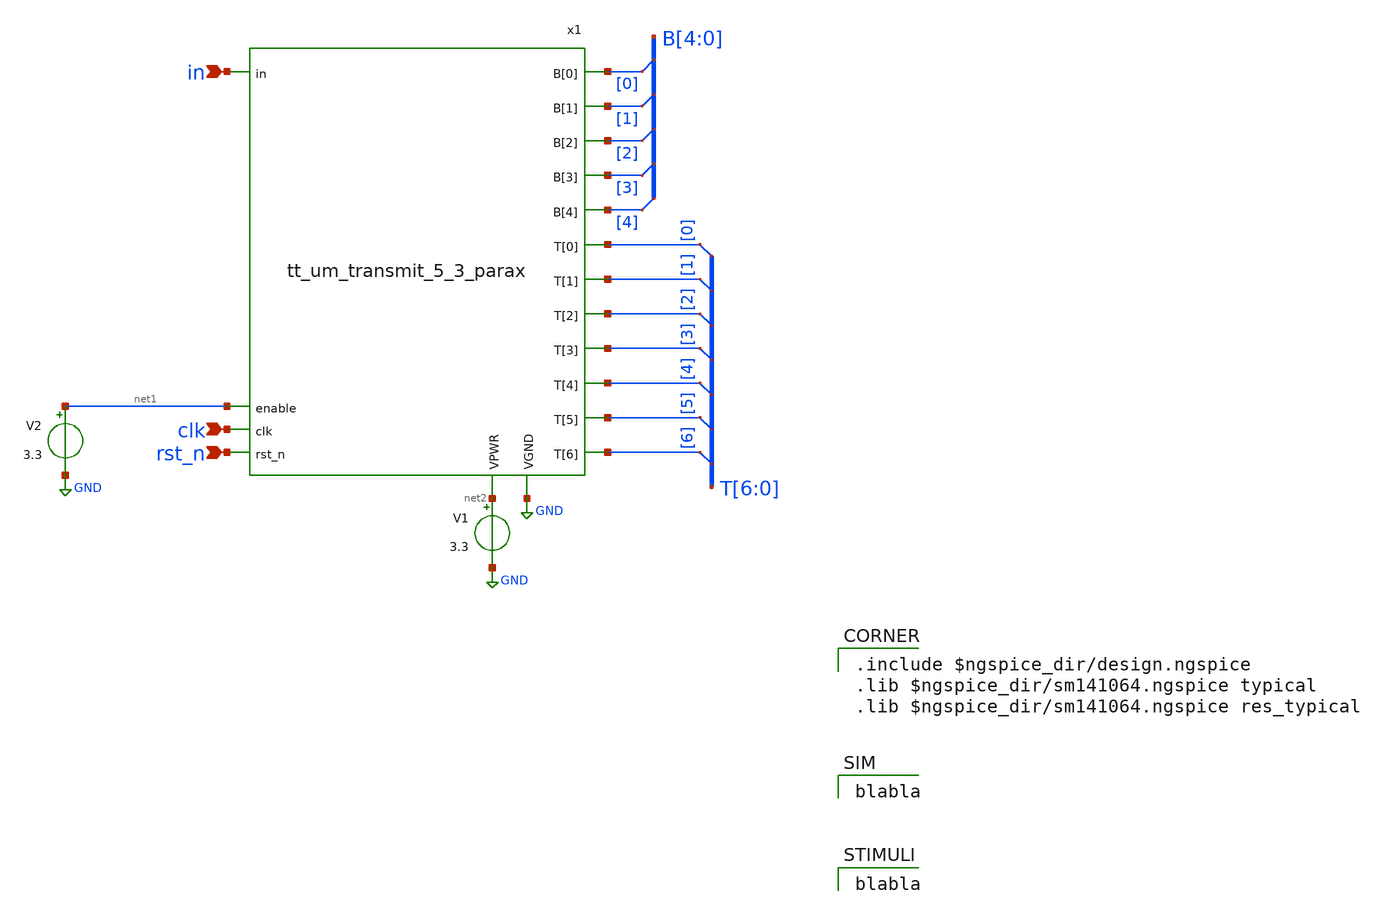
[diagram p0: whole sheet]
** sch_path: xschem/tb_transmit_5_3.sch
**.subckt tb_transmit_5_3 clk rst_n in
*.ipin clk
*.ipin rst_n
*.ipin in
x1 B[0] B[1] B[2] B[3] B[4] T[0] T[1] T[2] T[3] T[4] T[5] T[6] in GND net2 net1 clk rst_n
+ tt_um_transmit_5_3_parax
V1 net2 GND 3.3
* tap: B[4:0] --> B[0]
* tap: B[4:0] --> B[1]
* tap: B[4:0] --> B[2]
* tap: B[4:0] --> B[3]
* tap: B[4:0] --> B[4]
* tap: T[6:0] --> T[0]
* tap: T[6:0] --> T[1]
* tap: T[6:0] --> T[2]
* tap: T[6:0] --> T[3]
* tap: T[6:0] --> T[4]
* tap: T[6:0] --> T[5]
* tap: T[6:0] --> T[6]
V2 net1 GND 3.3
**** begin user architecture code

.include $ngspice_dir/design.ngspice
.lib $ngspice_dir/sm141064.ngspice typical
.lib $ngspice_dir/sm141064.ngspice res_typical


blabla


blabla

**** end user architecture code
**.ends

* expanding   symbol:  tt_um_transmit_5_3_parax.sym # of pins=18
** sym_path: xschem/tt_um_transmit_5_3_parax.sym
.include ../../mag/tt_um_transmit_5_3.sim.spice
.GLOBAL GND
.end
